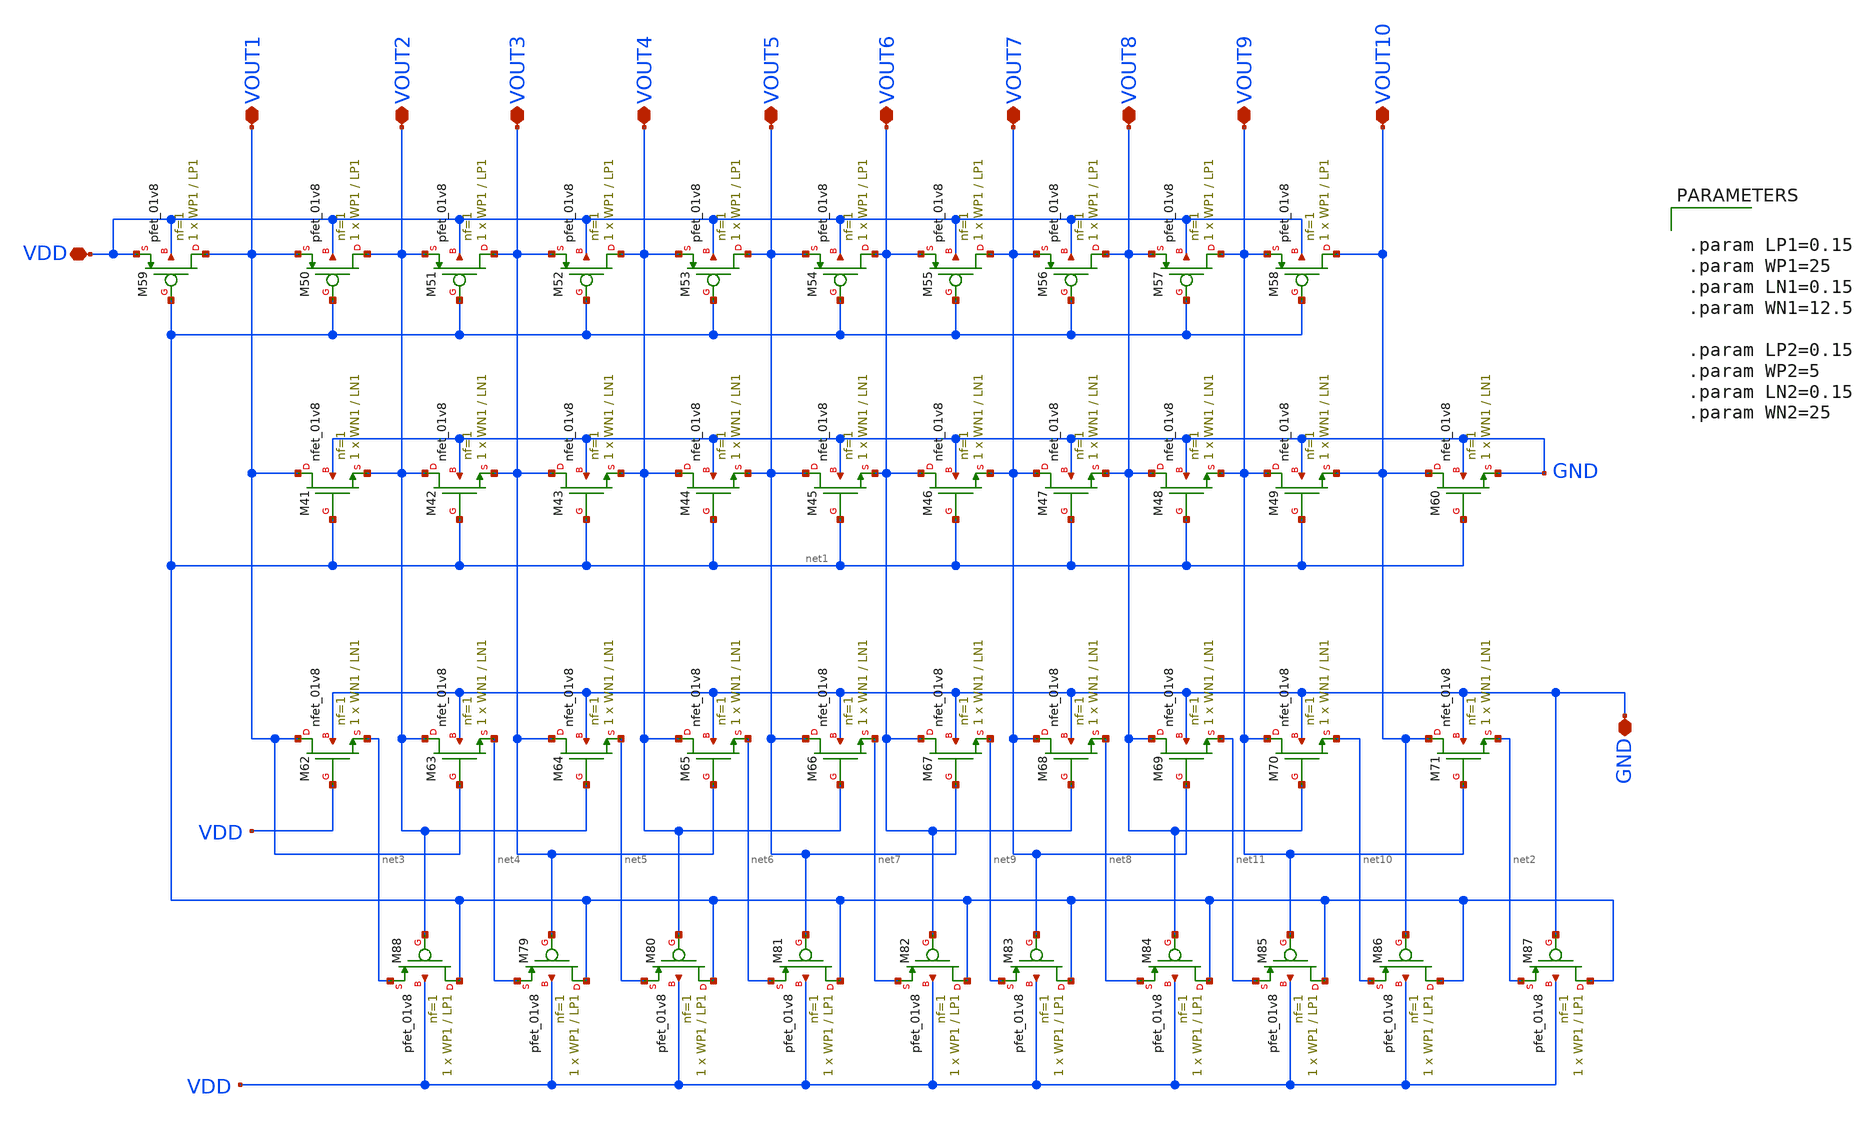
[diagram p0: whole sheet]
** sch_path: LIQAF circuit/10-Stage/10-stage_LDS.sch
**.subckt 10-stage_LDS VDD GND VOUT1 VOUT2 VOUT3 VOUT4 VOUT5 VOUT6 VOUT7 VOUT8 VOUT9 VOUT10
*.iopin VDD
*.iopin GND
*.iopin VOUT1
*.iopin VOUT2
*.iopin VOUT3
*.iopin VOUT4
*.iopin VOUT5
*.iopin VOUT6
*.iopin VOUT7
*.iopin VOUT8
*.iopin VOUT9
*.iopin VOUT10
XM41 VOUT1 net1 VOUT2 GND sky130_fd_pr__nfet_01v8 L=LN1 W=WN1 nf=1 ad='int((nf+1)/2) * W/nf * 0.29' as='int((nf+2)/2) * W/nf * 0.29'
+ pd='2*int((nf+1)/2) * (W/nf + 0.29)' ps='2*int((nf+2)/2) * (W/nf + 0.29)' nrd='0.29 / W' nrs='0.29 / W'
+ sa=0 sb=0 sd=0 mult=1 m=1
XM42 VOUT2 net1 VOUT3 GND sky130_fd_pr__nfet_01v8 L=LN1 W=WN1 nf=1 ad='int((nf+1)/2) * W/nf * 0.29' as='int((nf+2)/2) * W/nf * 0.29'
+ pd='2*int((nf+1)/2) * (W/nf + 0.29)' ps='2*int((nf+2)/2) * (W/nf + 0.29)' nrd='0.29 / W' nrs='0.29 / W'
+ sa=0 sb=0 sd=0 mult=1 m=1
XM43 VOUT3 net1 VOUT4 GND sky130_fd_pr__nfet_01v8 L=LN1 W=WN1 nf=1 ad='int((nf+1)/2) * W/nf * 0.29' as='int((nf+2)/2) * W/nf * 0.29'
+ pd='2*int((nf+1)/2) * (W/nf + 0.29)' ps='2*int((nf+2)/2) * (W/nf + 0.29)' nrd='0.29 / W' nrs='0.29 / W'
+ sa=0 sb=0 sd=0 mult=1 m=1
XM44 VOUT4 net1 VOUT5 GND sky130_fd_pr__nfet_01v8 L=LN1 W=WN1 nf=1 ad='int((nf+1)/2) * W/nf * 0.29' as='int((nf+2)/2) * W/nf * 0.29'
+ pd='2*int((nf+1)/2) * (W/nf + 0.29)' ps='2*int((nf+2)/2) * (W/nf + 0.29)' nrd='0.29 / W' nrs='0.29 / W'
+ sa=0 sb=0 sd=0 mult=1 m=1
XM45 VOUT5 net1 VOUT6 GND sky130_fd_pr__nfet_01v8 L=LN1 W=WN1 nf=1 ad='int((nf+1)/2) * W/nf * 0.29' as='int((nf+2)/2) * W/nf * 0.29'
+ pd='2*int((nf+1)/2) * (W/nf + 0.29)' ps='2*int((nf+2)/2) * (W/nf + 0.29)' nrd='0.29 / W' nrs='0.29 / W'
+ sa=0 sb=0 sd=0 mult=1 m=1
XM46 VOUT6 net1 VOUT7 GND sky130_fd_pr__nfet_01v8 L=LN1 W=WN1 nf=1 ad='int((nf+1)/2) * W/nf * 0.29' as='int((nf+2)/2) * W/nf * 0.29'
+ pd='2*int((nf+1)/2) * (W/nf + 0.29)' ps='2*int((nf+2)/2) * (W/nf + 0.29)' nrd='0.29 / W' nrs='0.29 / W'
+ sa=0 sb=0 sd=0 mult=1 m=1
XM47 VOUT7 net1 VOUT8 GND sky130_fd_pr__nfet_01v8 L=LN1 W=WN1 nf=1 ad='int((nf+1)/2) * W/nf * 0.29' as='int((nf+2)/2) * W/nf * 0.29'
+ pd='2*int((nf+1)/2) * (W/nf + 0.29)' ps='2*int((nf+2)/2) * (W/nf + 0.29)' nrd='0.29 / W' nrs='0.29 / W'
+ sa=0 sb=0 sd=0 mult=1 m=1
XM48 VOUT8 net1 VOUT9 GND sky130_fd_pr__nfet_01v8 L=LN1 W=WN1 nf=1 ad='int((nf+1)/2) * W/nf * 0.29' as='int((nf+2)/2) * W/nf * 0.29'
+ pd='2*int((nf+1)/2) * (W/nf + 0.29)' ps='2*int((nf+2)/2) * (W/nf + 0.29)' nrd='0.29 / W' nrs='0.29 / W'
+ sa=0 sb=0 sd=0 mult=1 m=1
XM49 VOUT9 net1 VOUT10 GND sky130_fd_pr__nfet_01v8 L=LN1 W=WN1 nf=1 ad='int((nf+1)/2) * W/nf * 0.29'
+ as='int((nf+2)/2) * W/nf * 0.29' pd='2*int((nf+1)/2) * (W/nf + 0.29)' ps='2*int((nf+2)/2) * (W/nf + 0.29)'
+ nrd='0.29 / W' nrs='0.29 / W' sa=0 sb=0 sd=0 mult=1 m=1
XM50 VOUT2 net1 VOUT1 VDD sky130_fd_pr__pfet_01v8 L=LP1 W=WP1 nf=1 ad='int((nf+1)/2) * W/nf * 0.29' as='int((nf+2)/2) * W/nf * 0.29'
+ pd='2*int((nf+1)/2) * (W/nf + 0.29)' ps='2*int((nf+2)/2) * (W/nf + 0.29)' nrd='0.29 / W' nrs='0.29 / W'
+ sa=0 sb=0 sd=0 mult=1 m=1
XM51 VOUT3 net1 VOUT2 VDD sky130_fd_pr__pfet_01v8 L=LP1 W=WP1 nf=1 ad='int((nf+1)/2) * W/nf * 0.29' as='int((nf+2)/2) * W/nf * 0.29'
+ pd='2*int((nf+1)/2) * (W/nf + 0.29)' ps='2*int((nf+2)/2) * (W/nf + 0.29)' nrd='0.29 / W' nrs='0.29 / W'
+ sa=0 sb=0 sd=0 mult=1 m=1
XM52 VOUT4 net1 VOUT3 VDD sky130_fd_pr__pfet_01v8 L=LP1 W=WP1 nf=1 ad='int((nf+1)/2) * W/nf * 0.29' as='int((nf+2)/2) * W/nf * 0.29'
+ pd='2*int((nf+1)/2) * (W/nf + 0.29)' ps='2*int((nf+2)/2) * (W/nf + 0.29)' nrd='0.29 / W' nrs='0.29 / W'
+ sa=0 sb=0 sd=0 mult=1 m=1
XM53 VOUT5 net1 VOUT4 VDD sky130_fd_pr__pfet_01v8 L=LP1 W=WP1 nf=1 ad='int((nf+1)/2) * W/nf * 0.29' as='int((nf+2)/2) * W/nf * 0.29'
+ pd='2*int((nf+1)/2) * (W/nf + 0.29)' ps='2*int((nf+2)/2) * (W/nf + 0.29)' nrd='0.29 / W' nrs='0.29 / W'
+ sa=0 sb=0 sd=0 mult=1 m=1
XM54 VOUT6 net1 VOUT5 VDD sky130_fd_pr__pfet_01v8 L=LP1 W=WP1 nf=1 ad='int((nf+1)/2) * W/nf * 0.29' as='int((nf+2)/2) * W/nf * 0.29'
+ pd='2*int((nf+1)/2) * (W/nf + 0.29)' ps='2*int((nf+2)/2) * (W/nf + 0.29)' nrd='0.29 / W' nrs='0.29 / W'
+ sa=0 sb=0 sd=0 mult=1 m=1
XM55 VOUT7 net1 VOUT6 VDD sky130_fd_pr__pfet_01v8 L=LP1 W=WP1 nf=1 ad='int((nf+1)/2) * W/nf * 0.29' as='int((nf+2)/2) * W/nf * 0.29'
+ pd='2*int((nf+1)/2) * (W/nf + 0.29)' ps='2*int((nf+2)/2) * (W/nf + 0.29)' nrd='0.29 / W' nrs='0.29 / W'
+ sa=0 sb=0 sd=0 mult=1 m=1
XM56 VOUT8 net1 VOUT7 VDD sky130_fd_pr__pfet_01v8 L=LP1 W=WP1 nf=1 ad='int((nf+1)/2) * W/nf * 0.29' as='int((nf+2)/2) * W/nf * 0.29'
+ pd='2*int((nf+1)/2) * (W/nf + 0.29)' ps='2*int((nf+2)/2) * (W/nf + 0.29)' nrd='0.29 / W' nrs='0.29 / W'
+ sa=0 sb=0 sd=0 mult=1 m=1
XM57 VOUT9 net1 VOUT8 VDD sky130_fd_pr__pfet_01v8 L=LP1 W=WP1 nf=1 ad='int((nf+1)/2) * W/nf * 0.29' as='int((nf+2)/2) * W/nf * 0.29'
+ pd='2*int((nf+1)/2) * (W/nf + 0.29)' ps='2*int((nf+2)/2) * (W/nf + 0.29)' nrd='0.29 / W' nrs='0.29 / W'
+ sa=0 sb=0 sd=0 mult=1 m=1
XM58 VOUT10 net1 VOUT9 VDD sky130_fd_pr__pfet_01v8 L=LP1 W=WP1 nf=1 ad='int((nf+1)/2) * W/nf * 0.29'
+ as='int((nf+2)/2) * W/nf * 0.29' pd='2*int((nf+1)/2) * (W/nf + 0.29)' ps='2*int((nf+2)/2) * (W/nf + 0.29)'
+ nrd='0.29 / W' nrs='0.29 / W' sa=0 sb=0 sd=0 mult=1 m=1
XM59 VOUT1 net1 VDD VDD sky130_fd_pr__pfet_01v8 L=LP1 W=WP1 nf=1 ad='int((nf+1)/2) * W/nf * 0.29' as='int((nf+2)/2) * W/nf * 0.29'
+ pd='2*int((nf+1)/2) * (W/nf + 0.29)' ps='2*int((nf+2)/2) * (W/nf + 0.29)' nrd='0.29 / W' nrs='0.29 / W'
+ sa=0 sb=0 sd=0 mult=1 m=1
XM60 VOUT10 net1 GND GND sky130_fd_pr__nfet_01v8 L=LN1 W=WN1 nf=1 ad='int((nf+1)/2) * W/nf * 0.29' as='int((nf+2)/2) * W/nf * 0.29'
+ pd='2*int((nf+1)/2) * (W/nf + 0.29)' ps='2*int((nf+2)/2) * (W/nf + 0.29)' nrd='0.29 / W' nrs='0.29 / W'
+ sa=0 sb=0 sd=0 mult=1 m=1
XM62 VOUT1 VDD net3 GND sky130_fd_pr__nfet_01v8 L=LN1 W=WN1 nf=1 ad='int((nf+1)/2) * W/nf * 0.29' as='int((nf+2)/2) * W/nf * 0.29'
+ pd='2*int((nf+1)/2) * (W/nf + 0.29)' ps='2*int((nf+2)/2) * (W/nf + 0.29)' nrd='0.29 / W' nrs='0.29 / W'
+ sa=0 sb=0 sd=0 mult=1 m=1
XM63 VOUT2 VOUT1 net4 GND sky130_fd_pr__nfet_01v8 L=LN1 W=WN1 nf=1 ad='int((nf+1)/2) * W/nf * 0.29' as='int((nf+2)/2) * W/nf * 0.29'
+ pd='2*int((nf+1)/2) * (W/nf + 0.29)' ps='2*int((nf+2)/2) * (W/nf + 0.29)' nrd='0.29 / W' nrs='0.29 / W'
+ sa=0 sb=0 sd=0 mult=1 m=1
XM64 VOUT3 VOUT2 net5 GND sky130_fd_pr__nfet_01v8 L=LN1 W=WN1 nf=1 ad='int((nf+1)/2) * W/nf * 0.29' as='int((nf+2)/2) * W/nf * 0.29'
+ pd='2*int((nf+1)/2) * (W/nf + 0.29)' ps='2*int((nf+2)/2) * (W/nf + 0.29)' nrd='0.29 / W' nrs='0.29 / W'
+ sa=0 sb=0 sd=0 mult=1 m=1
XM65 VOUT4 VOUT3 net6 GND sky130_fd_pr__nfet_01v8 L=LN1 W=WN1 nf=1 ad='int((nf+1)/2) * W/nf * 0.29' as='int((nf+2)/2) * W/nf * 0.29'
+ pd='2*int((nf+1)/2) * (W/nf + 0.29)' ps='2*int((nf+2)/2) * (W/nf + 0.29)' nrd='0.29 / W' nrs='0.29 / W'
+ sa=0 sb=0 sd=0 mult=1 m=1
XM66 VOUT5 VOUT4 net7 GND sky130_fd_pr__nfet_01v8 L=LN1 W=WN1 nf=1 ad='int((nf+1)/2) * W/nf * 0.29' as='int((nf+2)/2) * W/nf * 0.29'
+ pd='2*int((nf+1)/2) * (W/nf + 0.29)' ps='2*int((nf+2)/2) * (W/nf + 0.29)' nrd='0.29 / W' nrs='0.29 / W'
+ sa=0 sb=0 sd=0 mult=1 m=1
XM67 VOUT6 VOUT5 net9 GND sky130_fd_pr__nfet_01v8 L=LN1 W=WN1 nf=1 ad='int((nf+1)/2) * W/nf * 0.29' as='int((nf+2)/2) * W/nf * 0.29'
+ pd='2*int((nf+1)/2) * (W/nf + 0.29)' ps='2*int((nf+2)/2) * (W/nf + 0.29)' nrd='0.29 / W' nrs='0.29 / W'
+ sa=0 sb=0 sd=0 mult=1 m=1
XM68 VOUT7 VOUT6 net8 GND sky130_fd_pr__nfet_01v8 L=LN1 W=WN1 nf=1 ad='int((nf+1)/2) * W/nf * 0.29' as='int((nf+2)/2) * W/nf * 0.29'
+ pd='2*int((nf+1)/2) * (W/nf + 0.29)' ps='2*int((nf+2)/2) * (W/nf + 0.29)' nrd='0.29 / W' nrs='0.29 / W'
+ sa=0 sb=0 sd=0 mult=1 m=1
XM69 VOUT8 VOUT7 net11 GND sky130_fd_pr__nfet_01v8 L=LN1 W=WN1 nf=1 ad='int((nf+1)/2) * W/nf * 0.29'
+ as='int((nf+2)/2) * W/nf * 0.29' pd='2*int((nf+1)/2) * (W/nf + 0.29)' ps='2*int((nf+2)/2) * (W/nf + 0.29)'
+ nrd='0.29 / W' nrs='0.29 / W' sa=0 sb=0 sd=0 mult=1 m=1
XM70 VOUT9 VOUT8 net10 GND sky130_fd_pr__nfet_01v8 L=LN1 W=WN1 nf=1 ad='int((nf+1)/2) * W/nf * 0.29'
+ as='int((nf+2)/2) * W/nf * 0.29' pd='2*int((nf+1)/2) * (W/nf + 0.29)' ps='2*int((nf+2)/2) * (W/nf + 0.29)'
+ nrd='0.29 / W' nrs='0.29 / W' sa=0 sb=0 sd=0 mult=1 m=1
XM71 VOUT10 VOUT9 net2 GND sky130_fd_pr__nfet_01v8 L=LN1 W=WN1 nf=1 ad='int((nf+1)/2) * W/nf * 0.29'
+ as='int((nf+2)/2) * W/nf * 0.29' pd='2*int((nf+1)/2) * (W/nf + 0.29)' ps='2*int((nf+2)/2) * (W/nf + 0.29)'
+ nrd='0.29 / W' nrs='0.29 / W' sa=0 sb=0 sd=0 mult=1 m=1
XM79 net1 VOUT3 net4 VDD sky130_fd_pr__pfet_01v8 L=LP1 W=WP1 nf=1 ad='int((nf+1)/2) * W/nf * 0.29' as='int((nf+2)/2) * W/nf * 0.29'
+ pd='2*int((nf+1)/2) * (W/nf + 0.29)' ps='2*int((nf+2)/2) * (W/nf + 0.29)' nrd='0.29 / W' nrs='0.29 / W'
+ sa=0 sb=0 sd=0 mult=1 m=1
XM80 net1 VOUT4 net5 VDD sky130_fd_pr__pfet_01v8 L=LP1 W=WP1 nf=1 ad='int((nf+1)/2) * W/nf * 0.29' as='int((nf+2)/2) * W/nf * 0.29'
+ pd='2*int((nf+1)/2) * (W/nf + 0.29)' ps='2*int((nf+2)/2) * (W/nf + 0.29)' nrd='0.29 / W' nrs='0.29 / W'
+ sa=0 sb=0 sd=0 mult=1 m=1
XM81 net1 VOUT5 net6 VDD sky130_fd_pr__pfet_01v8 L=LP1 W=WP1 nf=1 ad='int((nf+1)/2) * W/nf * 0.29' as='int((nf+2)/2) * W/nf * 0.29'
+ pd='2*int((nf+1)/2) * (W/nf + 0.29)' ps='2*int((nf+2)/2) * (W/nf + 0.29)' nrd='0.29 / W' nrs='0.29 / W'
+ sa=0 sb=0 sd=0 mult=1 m=1
XM82 net1 VOUT6 net7 VDD sky130_fd_pr__pfet_01v8 L=LP1 W=WP1 nf=1 ad='int((nf+1)/2) * W/nf * 0.29' as='int((nf+2)/2) * W/nf * 0.29'
+ pd='2*int((nf+1)/2) * (W/nf + 0.29)' ps='2*int((nf+2)/2) * (W/nf + 0.29)' nrd='0.29 / W' nrs='0.29 / W'
+ sa=0 sb=0 sd=0 mult=1 m=1
XM83 net1 VOUT7 net9 VDD sky130_fd_pr__pfet_01v8 L=LP1 W=WP1 nf=1 ad='int((nf+1)/2) * W/nf * 0.29' as='int((nf+2)/2) * W/nf * 0.29'
+ pd='2*int((nf+1)/2) * (W/nf + 0.29)' ps='2*int((nf+2)/2) * (W/nf + 0.29)' nrd='0.29 / W' nrs='0.29 / W'
+ sa=0 sb=0 sd=0 mult=1 m=1
XM84 net1 VOUT8 net8 VDD sky130_fd_pr__pfet_01v8 L=LP1 W=WP1 nf=1 ad='int((nf+1)/2) * W/nf * 0.29' as='int((nf+2)/2) * W/nf * 0.29'
+ pd='2*int((nf+1)/2) * (W/nf + 0.29)' ps='2*int((nf+2)/2) * (W/nf + 0.29)' nrd='0.29 / W' nrs='0.29 / W'
+ sa=0 sb=0 sd=0 mult=1 m=1
XM85 net1 VOUT9 net11 VDD sky130_fd_pr__pfet_01v8 L=LP1 W=WP1 nf=1 ad='int((nf+1)/2) * W/nf * 0.29' as='int((nf+2)/2) * W/nf * 0.29'
+ pd='2*int((nf+1)/2) * (W/nf + 0.29)' ps='2*int((nf+2)/2) * (W/nf + 0.29)' nrd='0.29 / W' nrs='0.29 / W'
+ sa=0 sb=0 sd=0 mult=1 m=1
XM86 net1 VOUT10 net10 VDD sky130_fd_pr__pfet_01v8 L=LP1 W=WP1 nf=1 ad='int((nf+1)/2) * W/nf * 0.29'
+ as='int((nf+2)/2) * W/nf * 0.29' pd='2*int((nf+1)/2) * (W/nf + 0.29)' ps='2*int((nf+2)/2) * (W/nf + 0.29)'
+ nrd='0.29 / W' nrs='0.29 / W' sa=0 sb=0 sd=0 mult=1 m=1
XM87 net1 GND net2 VDD sky130_fd_pr__pfet_01v8 L=LP1 W=WP1 nf=1 ad='int((nf+1)/2) * W/nf * 0.29' as='int((nf+2)/2) * W/nf * 0.29'
+ pd='2*int((nf+1)/2) * (W/nf + 0.29)' ps='2*int((nf+2)/2) * (W/nf + 0.29)' nrd='0.29 / W' nrs='0.29 / W'
+ sa=0 sb=0 sd=0 mult=1 m=1
XM88 net1 VOUT2 net3 VDD sky130_fd_pr__pfet_01v8 L=LP1 W=WP1 nf=1 ad='int((nf+1)/2) * W/nf * 0.29' as='int((nf+2)/2) * W/nf * 0.29'
+ pd='2*int((nf+1)/2) * (W/nf + 0.29)' ps='2*int((nf+2)/2) * (W/nf + 0.29)' nrd='0.29 / W' nrs='0.29 / W'
+ sa=0 sb=0 sd=0 mult=1 m=1
**** begin user architecture code
 ** manual skywater pdks install (with patches applied)
* .lib $::SKYWATER_MODELS/models/sky130.lib.spice tt

** opencircuitdesign pdks install
.lib $::SKYWATER_MODELS/sky130.lib.spice tt

.param mc_mm_switch=0
.param mc_pr_switch=0
.param LP1=0.15



.param LP1=0.15
.param WP1=25
.param LN1=0.15
.param WN1=12.5

.param LP2=0.15
.param WP2=5
.param LN2=0.15
.param WN2=25


**** end user architecture code
**.ends
.end
